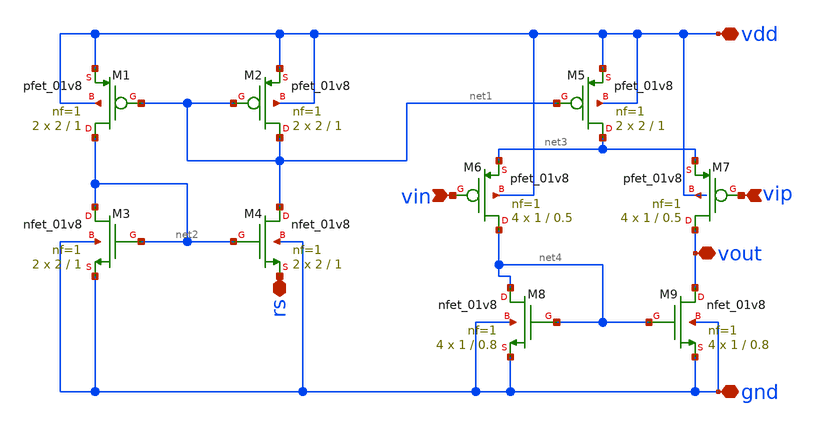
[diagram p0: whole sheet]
** sch_path: opamp/xschem/OpAmp.sch
**.subckt OpAmp vdd gnd rs vin vip vout
*.iopin vdd
*.iopin gnd
*.iopin rs
*.ipin vin
*.ipin vip
*.iopin vout
XM4 net1 net2 rs gnd sky130_fd_pr__nfet_01v8 L=1 W=2 nf=1 ad='int((nf+1)/2) * W/nf * 0.29' as='int((nf+2)/2) * W/nf * 0.29'
+ pd='2*int((nf+1)/2) * (W/nf + 0.29)' ps='2*int((nf+2)/2) * (W/nf + 0.29)' nrd='0.29 / W' nrs='0.29 / W'
+ sa=0 sb=0 sd=0 mult=2 m=2
XM3 net2 net2 gnd gnd sky130_fd_pr__nfet_01v8 L=1 W=2 nf=1 ad='int((nf+1)/2) * W/nf * 0.29' as='int((nf+2)/2) * W/nf * 0.29'
+ pd='2*int((nf+1)/2) * (W/nf + 0.29)' ps='2*int((nf+2)/2) * (W/nf + 0.29)' nrd='0.29 / W' nrs='0.29 / W'
+ sa=0 sb=0 sd=0 mult=2 m=2
XM9 vout net4 gnd gnd sky130_fd_pr__nfet_01v8 L=0.8 W=1 nf=1 ad='int((nf+1)/2) * W/nf * 0.29' as='int((nf+2)/2) * W/nf * 0.29'
+ pd='2*int((nf+1)/2) * (W/nf + 0.29)' ps='2*int((nf+2)/2) * (W/nf + 0.29)' nrd='0.29 / W' nrs='0.29 / W'
+ sa=0 sb=0 sd=0 mult=4 m=4
XM8 net4 net4 gnd gnd sky130_fd_pr__nfet_01v8 L=0.8 W=1 nf=1 ad='int((nf+1)/2) * W/nf * 0.29' as='int((nf+2)/2) * W/nf * 0.29'
+ pd='2*int((nf+1)/2) * (W/nf + 0.29)' ps='2*int((nf+2)/2) * (W/nf + 0.29)' nrd='0.29 / W' nrs='0.29 / W'
+ sa=0 sb=0 sd=0 mult=4 m=4
XM5 net3 net1 vdd vdd sky130_fd_pr__pfet_01v8 L=1 W=2 nf=1 ad='int((nf+1)/2) * W/nf * 0.29' as='int((nf+2)/2) * W/nf * 0.29'
+ pd='2*int((nf+1)/2) * (W/nf + 0.29)' ps='2*int((nf+2)/2) * (W/nf + 0.29)' nrd='0.29 / W' nrs='0.29 / W'
+ sa=0 sb=0 sd=0 mult=2 m=2
XM2 net1 net1 vdd vdd sky130_fd_pr__pfet_01v8 L=1 W=2 nf=1 ad='int((nf+1)/2) * W/nf * 0.29' as='int((nf+2)/2) * W/nf * 0.29'
+ pd='2*int((nf+1)/2) * (W/nf + 0.29)' ps='2*int((nf+2)/2) * (W/nf + 0.29)' nrd='0.29 / W' nrs='0.29 / W'
+ sa=0 sb=0 sd=0 mult=2 m=2
XM6 net4 vin net3 vdd sky130_fd_pr__pfet_01v8 L=0.5 W=1 nf=1 ad='int((nf+1)/2) * W/nf * 0.29' as='int((nf+2)/2) * W/nf * 0.29'
+ pd='2*int((nf+1)/2) * (W/nf + 0.29)' ps='2*int((nf+2)/2) * (W/nf + 0.29)' nrd='0.29 / W' nrs='0.29 / W'
+ sa=0 sb=0 sd=0 mult=4 m=4
XM7 vout vip net3 vdd sky130_fd_pr__pfet_01v8 L=0.5 W=1 nf=1 ad='int((nf+1)/2) * W/nf * 0.29' as='int((nf+2)/2) * W/nf * 0.29'
+ pd='2*int((nf+1)/2) * (W/nf + 0.29)' ps='2*int((nf+2)/2) * (W/nf + 0.29)' nrd='0.29 / W' nrs='0.29 / W'
+ sa=0 sb=0 sd=0 mult=4 m=4
XM1 net2 net1 vdd vdd sky130_fd_pr__pfet_01v8 L=1 W=2 nf=1 ad='int((nf+1)/2) * W/nf * 0.29' as='int((nf+2)/2) * W/nf * 0.29'
+ pd='2*int((nf+1)/2) * (W/nf + 0.29)' ps='2*int((nf+2)/2) * (W/nf + 0.29)' nrd='0.29 / W' nrs='0.29 / W'
+ sa=0 sb=0 sd=0 mult=2 m=2
**.ends
.end
